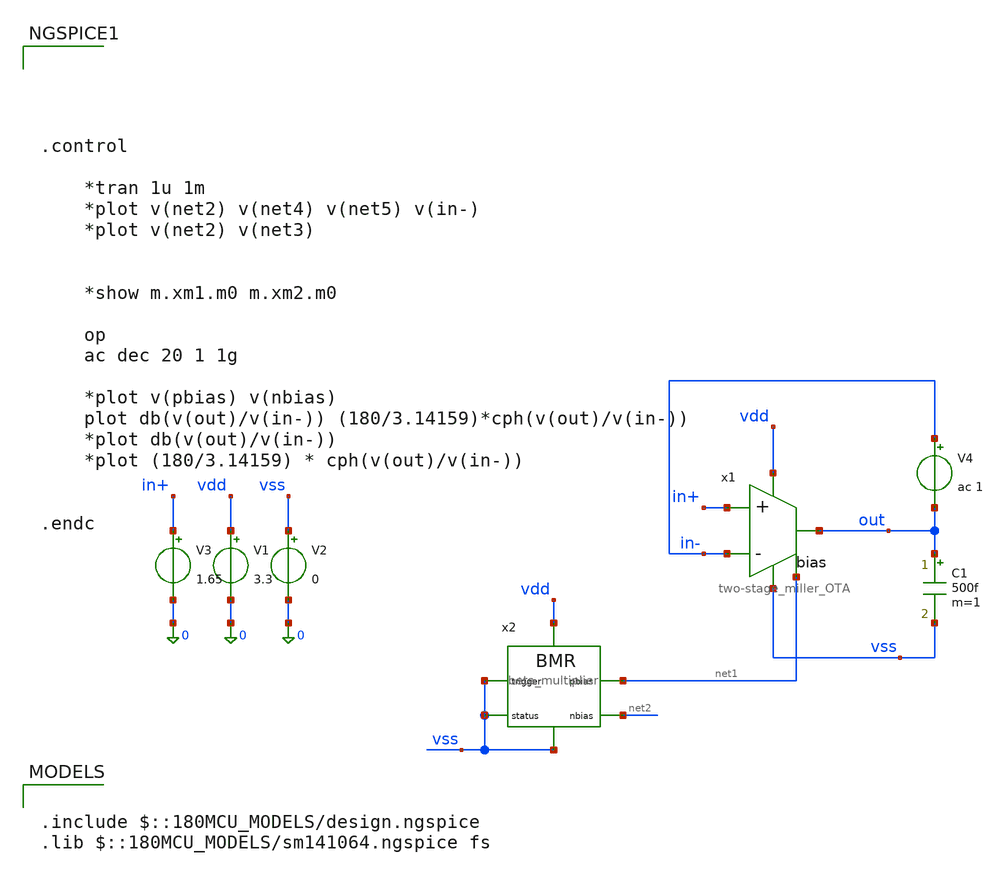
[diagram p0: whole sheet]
** sch_path: simulation/testbench_analog/OTA/OTA_freq-response.sch
**.subckt OTA_freq-response
V3 in+ 0 1.65
V1 vdd 0 3.3
V2 vss 0 0
V4 in- out ac 1
C1 out vss 500f m=1
x1 vdd out in+ in- net1 vss two-stage_miller_OTA
x2 vdd net1 net2 vss vss vss beta_multiplier
**** begin user architecture code





.control

	*tran 1u 1m
	*plot v(net2) v(net4) v(net5) v(in-)
	*plot v(net2) v(net3)


	*show m.xm1.m0 m.xm2.m0

	op
	ac dec 20 1 1g

	*plot v(pbias) v(nbias)
	plot db(v(out)/v(in-)) (180/3.14159)*cph(v(out)/v(in-))
	*plot db(v(out)/v(in-))
	*plot (180/3.14159) * cph(v(out)/v(in-))


.endc



.include $::180MCU_MODELS/design.ngspice
.lib $::180MCU_MODELS/sm141064.ngspice fs

**** end user architecture code
**.ends

* expanding   symbol:  acoustic-ranger-dvl-processor/design/analog/OTA/two-stage_miller_OTA.sym # of
*+ pins=6
** sym_path: design/analog/OTA/two-stage_miller_OTA.sym
** sch_path: design/analog/OTA/two-stage_miller_OTA.sch
.subckt two-stage_miller_OTA vdd out in+ in- bias vss
*.ipin in+
*.ipin in-
*.opin out
*.iopin vdd
*.iopin vss
*.ipin bias
XM1 net2 in- net1 vdd pfet_03v3 L=1u W=49.6u nf=1 ad='int((nf+1)/2) * W/nf * 0.18u' as='int((nf+2)/2) * W/nf * 0.18u'
+ pd='2*int((nf+1)/2) * (W/nf + 0.18u)' ps='2*int((nf+2)/2) * (W/nf + 0.18u)' nrd='0.18u / W' nrs='0.18u / W'
+ sa=0 sb=0 sd=0 m=1
XM2 net3 in+ net1 vdd pfet_03v3 L=1u W=49.6u nf=1 ad='int((nf+1)/2) * W/nf * 0.18u' as='int((nf+2)/2) * W/nf * 0.18u'
+ pd='2*int((nf+1)/2) * (W/nf + 0.18u)' ps='2*int((nf+2)/2) * (W/nf + 0.18u)' nrd='0.18u / W' nrs='0.18u / W'
+ sa=0 sb=0 sd=0 m=1
XM14 net3 net2 vss vss nfet_03v3 L=3u W=15.4u nf=1 ad='int((nf+1)/2) * W/nf * 0.18u' as='int((nf+2)/2) * W/nf * 0.18u'
+ pd='2*int((nf+1)/2) * (W/nf + 0.18u)' ps='2*int((nf+2)/2) * (W/nf + 0.18u)' nrd='0.18u / W' nrs='0.18u / W'
+ sa=0 sb=0 sd=0 m=1
XM15 net2 net2 vss vss nfet_03v3 L=3u W=15.4u nf=1 ad='int((nf+1)/2) * W/nf * 0.18u' as='int((nf+2)/2) * W/nf * 0.18u'
+ pd='2*int((nf+1)/2) * (W/nf + 0.18u)' ps='2*int((nf+2)/2) * (W/nf + 0.18u)' nrd='0.18u / W' nrs='0.18u / W'
+ sa=0 sb=0 sd=0 m=1
XM3 out net3 vss vss nfet_03v3 L=500n W=15.4u nf=1 ad='int((nf+1)/2) * W/nf * 0.18u' as='int((nf+2)/2) * W/nf * 0.18u'
+ pd='2*int((nf+1)/2) * (W/nf + 0.18u)' ps='2*int((nf+2)/2) * (W/nf + 0.18u)' nrd='0.18u / W' nrs='0.18u / W'
+ sa=0 sb=0 sd=0 m=1
C1 out net3 2pf m=1
XM4 net1 bias vdd vdd pfet_03v3 L=30u W=63.9u nf=1 ad='int((nf+1)/2) * W/nf * 0.18u' as='int((nf+2)/2) * W/nf * 0.18u'
+ pd='2*int((nf+1)/2) * (W/nf + 0.18u)' ps='2*int((nf+2)/2) * (W/nf + 0.18u)' nrd='0.18u / W' nrs='0.18u / W'
+ sa=0 sb=0 sd=0 m=6
XM5 out bias vdd vdd pfet_03v3 L=30u W=55.75u nf=1 ad='int((nf+1)/2) * W/nf * 0.18u' as='int((nf+2)/2) * W/nf * 0.18u'
+ pd='2*int((nf+1)/2) * (W/nf + 0.18u)' ps='2*int((nf+2)/2) * (W/nf + 0.18u)' nrd='0.18u / W' nrs='0.18u / W'
+ sa=0 sb=0 sd=0 m=15
.ends


* expanding   symbol:  acoustic-ranger-dvl-processor/design/analog/beta
*+ multiplier/beta_multiplier.sym # of pins=6
** sym_path: design/analog/beta multiplier/beta_multiplier.sym
** sch_path: design/analog/beta multiplier/beta_multiplier.sch
.subckt beta_multiplier vdd pbias nbias status trigger vss
*.iopin vdd
*.iopin vss
*.opin pbias
*.opin nbias
*.opin status
*.ipin trigger
XM1 pbias nbias net1 net1 nfet_03v3 L=30u W=51.28u nf=1 ad='int((nf+1)/2) * W/nf * 0.18u' as='int((nf+2)/2) * W/nf * 0.18u'
+ pd='2*int((nf+1)/2) * (W/nf + 0.18u)' ps='2*int((nf+2)/2) * (W/nf + 0.18u)' nrd='0.18u / W' nrs='0.18u / W'
+ sa=0 sb=0 sd=0 m=3
XM2 nbias nbias vss vss nfet_03v3 L=30u W=22.22u nf=1 ad='int((nf+1)/2) * W/nf * 0.18u' as='int((nf+2)/2) * W/nf * 0.18u'
+ pd='2*int((nf+1)/2) * (W/nf + 0.18u)' ps='2*int((nf+2)/2) * (W/nf + 0.18u)' nrd='0.18u / W' nrs='0.18u / W'
+ sa=0 sb=0 sd=0 m=3
XM3 pbias pbias vdd vdd pfet_03v3 L=30u W=52.08u nf=1 ad='int((nf+1)/2) * W/nf * 0.18u' as='int((nf+2)/2) * W/nf * 0.18u'
+ pd='2*int((nf+1)/2) * (W/nf + 0.18u)' ps='2*int((nf+2)/2) * (W/nf + 0.18u)' nrd='0.18u / W' nrs='0.18u / W'
+ sa=0 sb=0 sd=0 m=6
XM4 nbias pbias vdd vdd pfet_03v3 L=30u W=52.08u nf=1 ad='int((nf+1)/2) * W/nf * 0.18u' as='int((nf+2)/2) * W/nf * 0.18u'
+ pd='2*int((nf+1)/2) * (W/nf + 0.18u)' ps='2*int((nf+2)/2) * (W/nf + 0.18u)' nrd='0.18u / W' nrs='0.18u / W'
+ sa=0 sb=0 sd=0 m=6
R1 net1 vss 10k m=1
XM5 pbias trigger vss vss nfet_03v3 L=5u W=0.28u nf=1 ad='int((nf+1)/2) * W/nf * 0.18u' as='int((nf+2)/2) * W/nf * 0.18u'
+ pd='2*int((nf+1)/2) * (W/nf + 0.18u)' ps='2*int((nf+2)/2) * (W/nf + 0.18u)' nrd='0.18u / W' nrs='0.18u / W'
+ sa=0 sb=0 sd=0 m=1
XM10 net2 nbias vss vss nfet_03v3 L=0.28u W=18u nf=1 ad='int((nf+1)/2) * W/nf * 0.18u' as='int((nf+2)/2) * W/nf * 0.18u'
+ pd='2*int((nf+1)/2) * (W/nf + 0.18u)' ps='2*int((nf+2)/2) * (W/nf + 0.18u)' nrd='0.18u / W' nrs='0.18u / W'
+ sa=0 sb=0 sd=0 m=1
R3 vdd net2 10k m=1
XM11 status net2 vss vss nfet_03v3 L=1u W=1u nf=1 ad='int((nf+1)/2) * W/nf * 0.18u' as='int((nf+2)/2) * W/nf * 0.18u'
+ pd='2*int((nf+1)/2) * (W/nf + 0.18u)' ps='2*int((nf+2)/2) * (W/nf + 0.18u)' nrd='0.18u / W' nrs='0.18u / W'
+ sa=0 sb=0 sd=0 m=1
XM12 status net2 vdd vdd pfet_03v3 L=1u W=1u nf=1 ad='int((nf+1)/2) * W/nf * 0.18u' as='int((nf+2)/2) * W/nf * 0.18u'
+ pd='2*int((nf+1)/2) * (W/nf + 0.18u)' ps='2*int((nf+2)/2) * (W/nf + 0.18u)' nrd='0.18u / W' nrs='0.18u / W'
+ sa=0 sb=0 sd=0 m=1
.ends

.end
